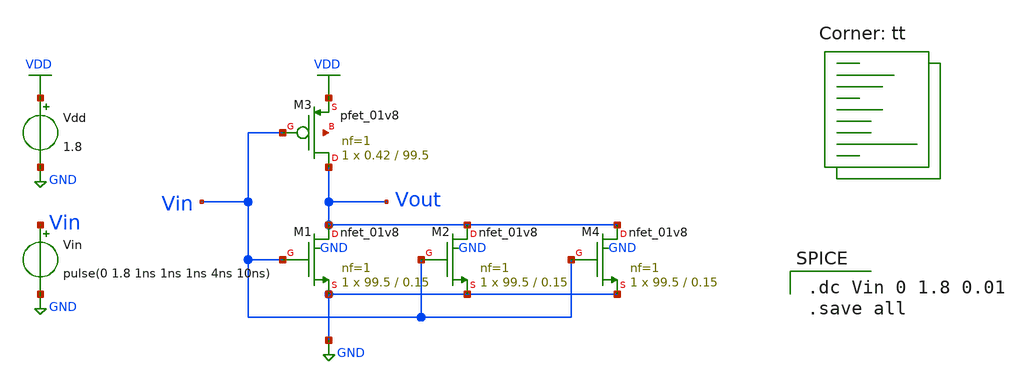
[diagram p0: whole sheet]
** sch_path: vdd1.8V/inverter_sat_1_trans.sch
**.subckt inverter_sat_1_trans
Vdd VDD GND 1.8
XM1 Vout Vin GND GND sky130_fd_pr__nfet_01v8 L=0.15 W=99.5 nf=1 ad='int((nf+1)/2) * W/nf * 0.29' as='int((nf+2)/2) * W/nf * 0.29'
+ pd='2*int((nf+1)/2) * (W/nf + 0.29)' ps='2*int((nf+2)/2) * (W/nf + 0.29)' nrd='0.29 / W' nrs='0.29 / W'
+ sa=0 sb=0 sd=0 mult=1 m=1
Vin Vin GND pulse(0 1.8 1ns 1ns 1ns 4ns 10ns)
XM3 Vout Vin VDD net1 sky130_fd_pr__pfet_01v8 L=99.5 W=0.42 nf=1 ad='int((nf+1)/2) * W/nf * 0.29' as='int((nf+2)/2) * W/nf * 0.29'
+ pd='2*int((nf+1)/2) * (W/nf + 0.29)' ps='2*int((nf+2)/2) * (W/nf + 0.29)' nrd='0.29 / W' nrs='0.29 / W'
+ sa=0 sb=0 sd=0 mult=1 m=1
XM2 Vout Vin GND GND sky130_fd_pr__nfet_01v8 L=0.15 W=99.5 nf=1 ad='int((nf+1)/2) * W/nf * 0.29' as='int((nf+2)/2) * W/nf * 0.29'
+ pd='2*int((nf+1)/2) * (W/nf + 0.29)' ps='2*int((nf+2)/2) * (W/nf + 0.29)' nrd='0.29 / W' nrs='0.29 / W'
+ sa=0 sb=0 sd=0 mult=1 m=1
XM4 Vout Vin GND GND sky130_fd_pr__nfet_01v8 L=0.15 W=99.5 nf=1 ad='int((nf+1)/2) * W/nf * 0.29' as='int((nf+2)/2) * W/nf * 0.29'
+ pd='2*int((nf+1)/2) * (W/nf + 0.29)' ps='2*int((nf+2)/2) * (W/nf + 0.29)' nrd='0.29 / W' nrs='0.29 / W'
+ sa=0 sb=0 sd=0 mult=1 m=1
**** begin user architecture code

.dc Vin 0 1.8 0.01
.save all

.lib $::SKYWATER_MODELS/sky130.lib.spice tt
**** end user architecture code
**.ends
.GLOBAL GND
.GLOBAL VDD
.end
